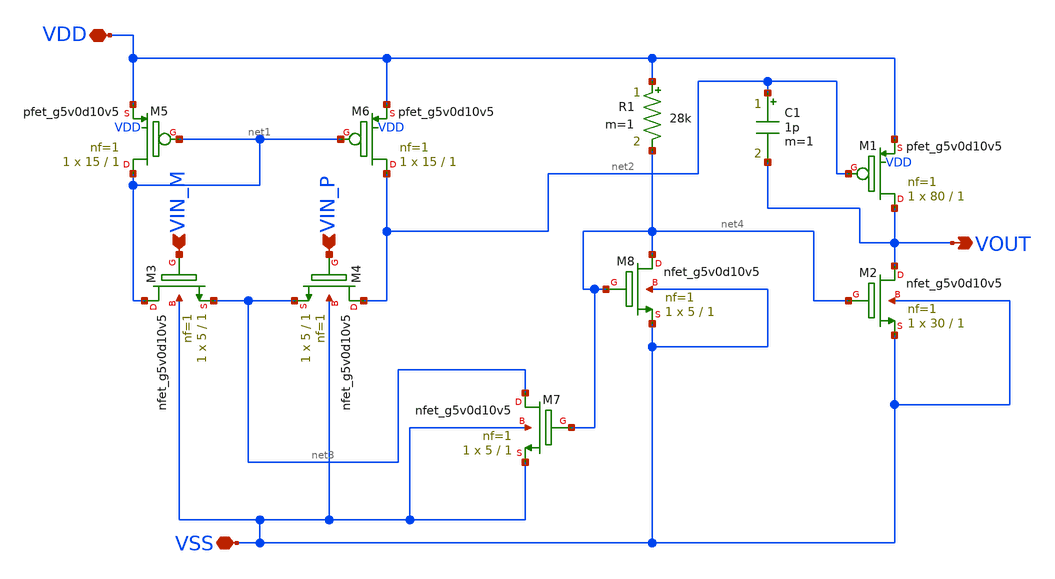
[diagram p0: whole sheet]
** sch_path: analog/schematics/opamp_two_stage.sch
**.subckt opamp_two_stage VIN_M VIN_P VDD VOUT VSS
*.ipin VIN_M
*.ipin VIN_P
*.iopin VDD
*.opin VOUT
*.iopin VSS
XM3 net1 VIN_M net3 VSS sky130_fd_pr__nfet_g5v0d10v5 L=1 W=5 nf=1 ad='int((nf+1)/2) * W/nf * 0.29' as='int((nf+2)/2) * W/nf * 0.29'
+ pd='2*int((nf+1)/2) * (W/nf + 0.29)' ps='2*int((nf+2)/2) * (W/nf + 0.29)' nrd='0.29 / W' nrs='0.29 / W'
+ sa=0 sb=0 sd=0 mult=1 m=1
XM4 net2 VIN_P net3 VSS sky130_fd_pr__nfet_g5v0d10v5 L=1 W=5 nf=1 ad='int((nf+1)/2) * W/nf * 0.29' as='int((nf+2)/2) * W/nf * 0.29'
+ pd='2*int((nf+1)/2) * (W/nf + 0.29)' ps='2*int((nf+2)/2) * (W/nf + 0.29)' nrd='0.29 / W' nrs='0.29 / W'
+ sa=0 sb=0 sd=0 mult=1 m=1
XM5 net1 net1 VDD VDD sky130_fd_pr__pfet_g5v0d10v5 L=1 W=15 nf=1 ad='int((nf+1)/2) * W/nf * 0.29' as='int((nf+2)/2) * W/nf * 0.29'
+ pd='2*int((nf+1)/2) * (W/nf + 0.29)' ps='2*int((nf+2)/2) * (W/nf + 0.29)' nrd='0.29 / W' nrs='0.29 / W'
+ sa=0 sb=0 sd=0 mult=1 m=1
XM6 net2 net1 VDD VDD sky130_fd_pr__pfet_g5v0d10v5 L=1 W=15 nf=1 ad='int((nf+1)/2) * W/nf * 0.29' as='int((nf+2)/2) * W/nf * 0.29'
+ pd='2*int((nf+1)/2) * (W/nf + 0.29)' ps='2*int((nf+2)/2) * (W/nf + 0.29)' nrd='0.29 / W' nrs='0.29 / W'
+ sa=0 sb=0 sd=0 mult=1 m=1
XM7 net3 net4 VSS VSS sky130_fd_pr__nfet_g5v0d10v5 L=1 W=5 nf=1 ad='int((nf+1)/2) * W/nf * 0.29' as='int((nf+2)/2) * W/nf * 0.29'
+ pd='2*int((nf+1)/2) * (W/nf + 0.29)' ps='2*int((nf+2)/2) * (W/nf + 0.29)' nrd='0.29 / W' nrs='0.29 / W'
+ sa=0 sb=0 sd=0 mult=1 m=1
R1 VDD net4 28k m=1
C1 net2 VOUT 1p m=1
XM8 net4 net4 VSS VSS sky130_fd_pr__nfet_g5v0d10v5 L=1 W=5 nf=1 ad='int((nf+1)/2) * W/nf * 0.29' as='int((nf+2)/2) * W/nf * 0.29'
+ pd='2*int((nf+1)/2) * (W/nf + 0.29)' ps='2*int((nf+2)/2) * (W/nf + 0.29)' nrd='0.29 / W' nrs='0.29 / W'
+ sa=0 sb=0 sd=0 mult=1 m=1
XM1 VOUT net2 VDD VDD sky130_fd_pr__pfet_g5v0d10v5 L=1 W=80 nf=1 ad='int((nf+1)/2) * W/nf * 0.29' as='int((nf+2)/2) * W/nf * 0.29'
+ pd='2*int((nf+1)/2) * (W/nf + 0.29)' ps='2*int((nf+2)/2) * (W/nf + 0.29)' nrd='0.29 / W' nrs='0.29 / W'
+ sa=0 sb=0 sd=0 mult=1 m=1
XM2 VOUT net4 VSS VSS sky130_fd_pr__nfet_g5v0d10v5 L=1 W=30 nf=1 ad='int((nf+1)/2) * W/nf * 0.29' as='int((nf+2)/2) * W/nf * 0.29'
+ pd='2*int((nf+1)/2) * (W/nf + 0.29)' ps='2*int((nf+2)/2) * (W/nf + 0.29)' nrd='0.29 / W' nrs='0.29 / W'
+ sa=0 sb=0 sd=0 mult=1 m=1
**.ends
.end
